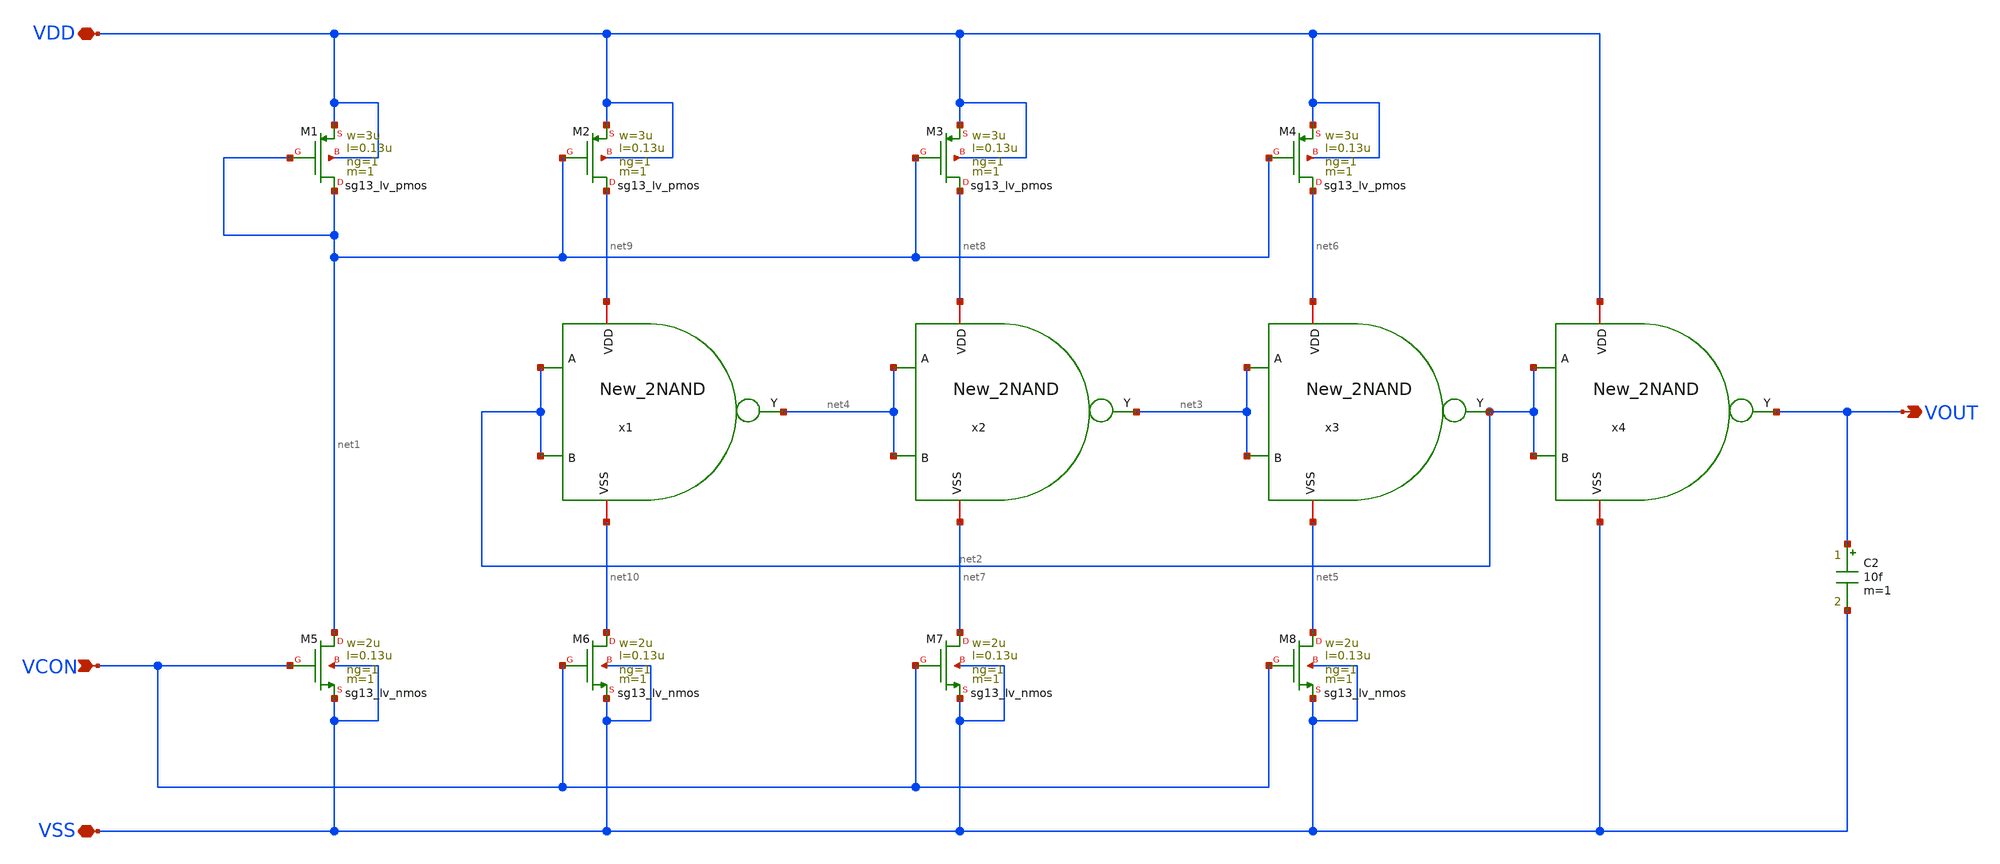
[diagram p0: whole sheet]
** sch_path: Team 1 Design/design_data/xschem/VCO/VCO_3Stages.sch
**.subckt VCO_3Stages VDD VSS VCON VOUT
*.iopin VDD
*.iopin VSS
*.ipin VCON
*.opin VOUT
XM1 net1 net1 VDD VDD sg13_lv_pmos w=3u l=0.13u ng=1 m=1 mm_ok=1
XM2 net9 net1 VDD VDD sg13_lv_pmos w=3u l=0.13u ng=1 m=1 mm_ok=1
XM3 net8 net1 VDD VDD sg13_lv_pmos w=3u l=0.13u ng=1 m=1 mm_ok=1
XM4 net6 net1 VDD VDD sg13_lv_pmos w=3u l=0.13u ng=1 m=1 mm_ok=1
XM5 net1 VCON VSS VSS sg13_lv_nmos w=2u l=0.13u ng=1 m=1 mm_ok=1
XM6 net10 VCON VSS VSS sg13_lv_nmos w=2u l=0.13u ng=1 m=1 mm_ok=1
XM7 net7 VCON VSS VSS sg13_lv_nmos w=2u l=0.13u ng=1 m=1 mm_ok=1
XM8 net5 VCON VSS VSS sg13_lv_nmos w=2u l=0.13u ng=1 m=1 mm_ok=1
C2 VOUT VSS 10f m=1
x1 net9 net10 net2 net4 net2 New_2NAND
x2 net8 net7 net4 net3 net4 New_2NAND
x3 net6 net5 net3 net2 net3 New_2NAND
x4 VDD VSS net2 VOUT net2 New_2NAND
**.ends

* expanding   symbol:  /foss/designs/Team1/New_2NAND/New_2NAND.sym # of pins=5
** sym_path: Team 1 Design/design_data/xschem/2_Input_NAND_New/New_2NAND.sym
** sch_path: Team 1 Design/design_data/xschem/2_Input_NAND_New/New_2NAND.sch
.subckt New_2NAND VDD VSS A Y B
*.ipin B
*.opin Y
*.ipin A
*.iopin VDD
*.iopin VSS
XM1 Y A VDD VDD sg13_lv_pmos w=3u l=0.13u ng=1 m=1 mm_ok=1
XM2 Y B VDD VDD sg13_lv_pmos w=3u l=0.13u ng=1 m=1 mm_ok=1
XM3 Y B net1 VSS sg13_lv_nmos w=2u l=0.13u ng=1 m=1 mm_ok=1
XM4 net1 A VSS VSS sg13_lv_nmos w=2u l=0.13u ng=1 m=1 mm_ok=1
.ends

.end
